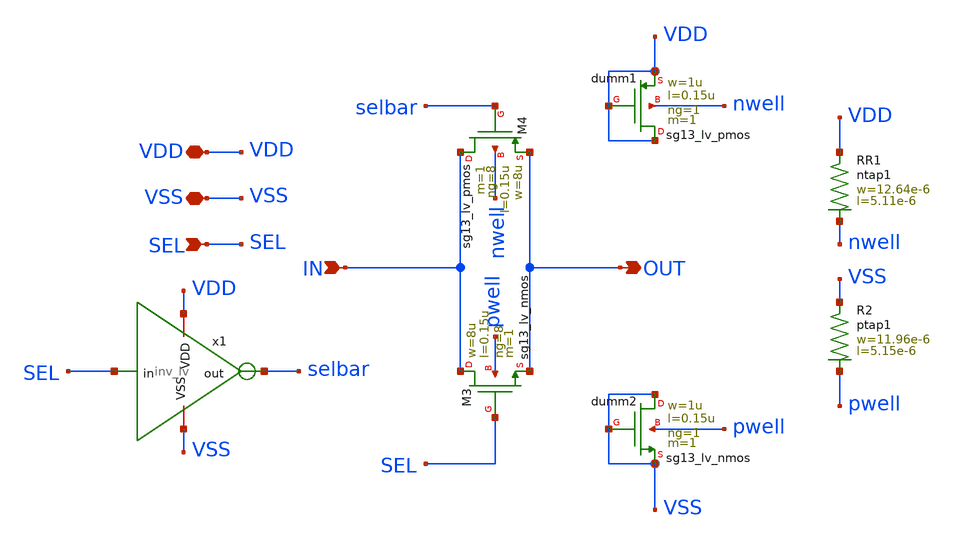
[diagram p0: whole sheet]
** sch_path: xschem/tg_lv.sch
**.subckt tg_lv IN VDD VSS OUT SEL
*.ipin IN
*.iopin VDD
*.iopin VSS
*.opin OUT
*.ipin SEL
x1 VDD SEL selbar VSS inv_lv
XM3 IN SEL OUT pwell sg13_lv_nmos w=8u l=0.15u ng=8 m=1 mm_ok=1
XM4 IN selbar OUT nwell sg13_lv_pmos w=8u l=0.15u ng=8 m=1 mm_ok=1
Xdumm1 VDD VDD VDD nwell sg13_lv_pmos w=1u l=0.15u ng=1 m=1 mm_ok=1
Xdumm2 VSS VSS VSS pwell sg13_lv_nmos w=1u l=0.15u ng=1 m=1 mm_ok=1
XR1 VDD nwell ntap1 R=9.791 w=12.64e-6 l=5.11e-6
XR2 VSS pwell ptap1 R=10.23 w=11.96e-6 l=5.15e-6
**.ends

* expanding   symbol:  inv_lv.sym # of pins=4
** sym_path: inv_lv.sym
** sch_path: inv_lv.sch
.subckt inv_lv VDD in out VSS
*.ipin in
*.opin out
*.iopin VDD
*.iopin VSS
XM3 out in VDD nwell sg13_lv_pmos w=1u l=0.15u ng=1 m=1 mm_ok=1
XM4 out in VSS pwell sg13_lv_nmos w=1u l=0.15u ng=1 m=1 mm_ok=1
Xdumm1 VDD VDD VDD nwell sg13_lv_pmos w=1u l=0.15u ng=1 m=1 mm_ok=1
Xdumm2 VSS VSS VSS pwell sg13_lv_nmos w=1u l=0.15u ng=1 m=1 mm_ok=1
XR1 VDD nwell ntap1 R=14.47 w=8.09e-6 l=5.11e-6
XR2 VSS pwell ptap1 R=15.49 w=7.41e-6 l=5.15e-6
.ends

.end
